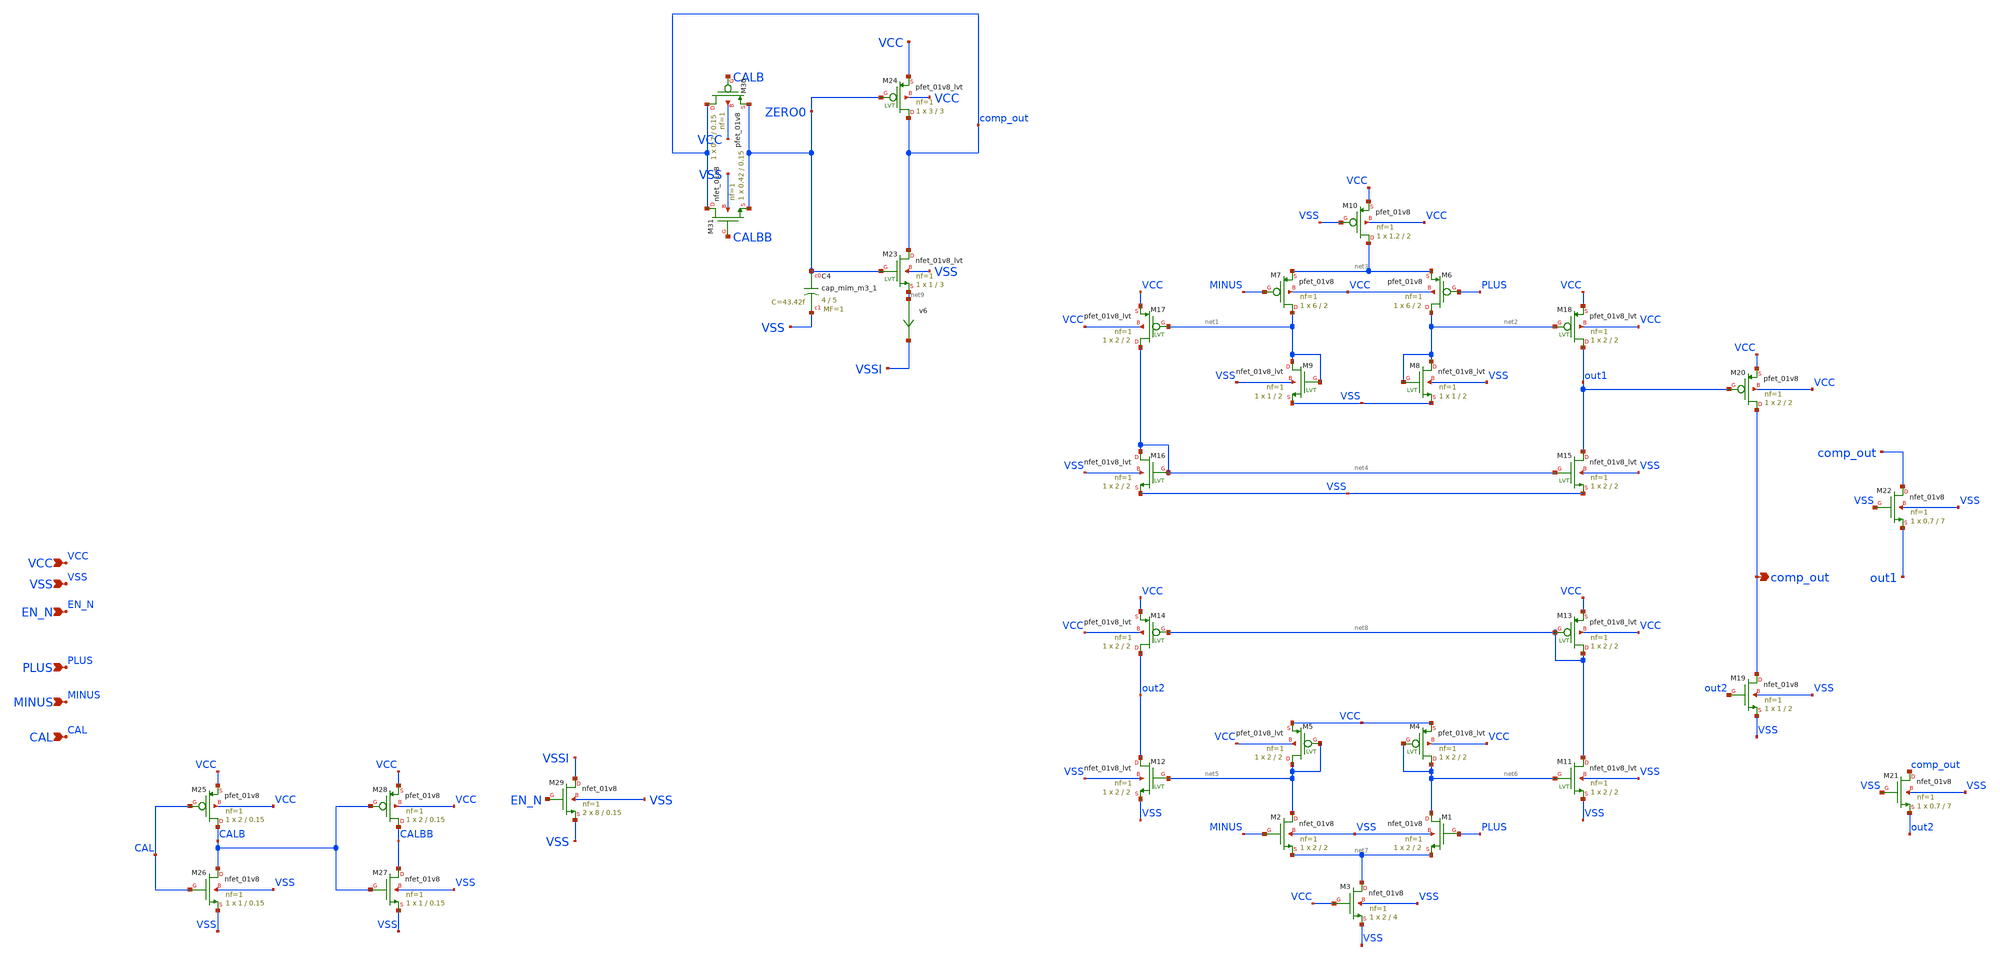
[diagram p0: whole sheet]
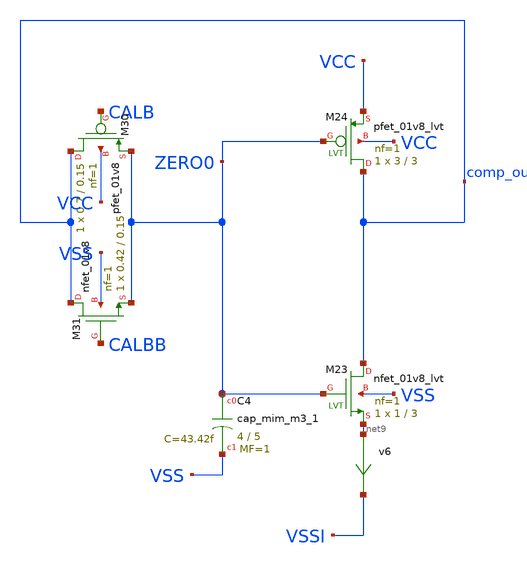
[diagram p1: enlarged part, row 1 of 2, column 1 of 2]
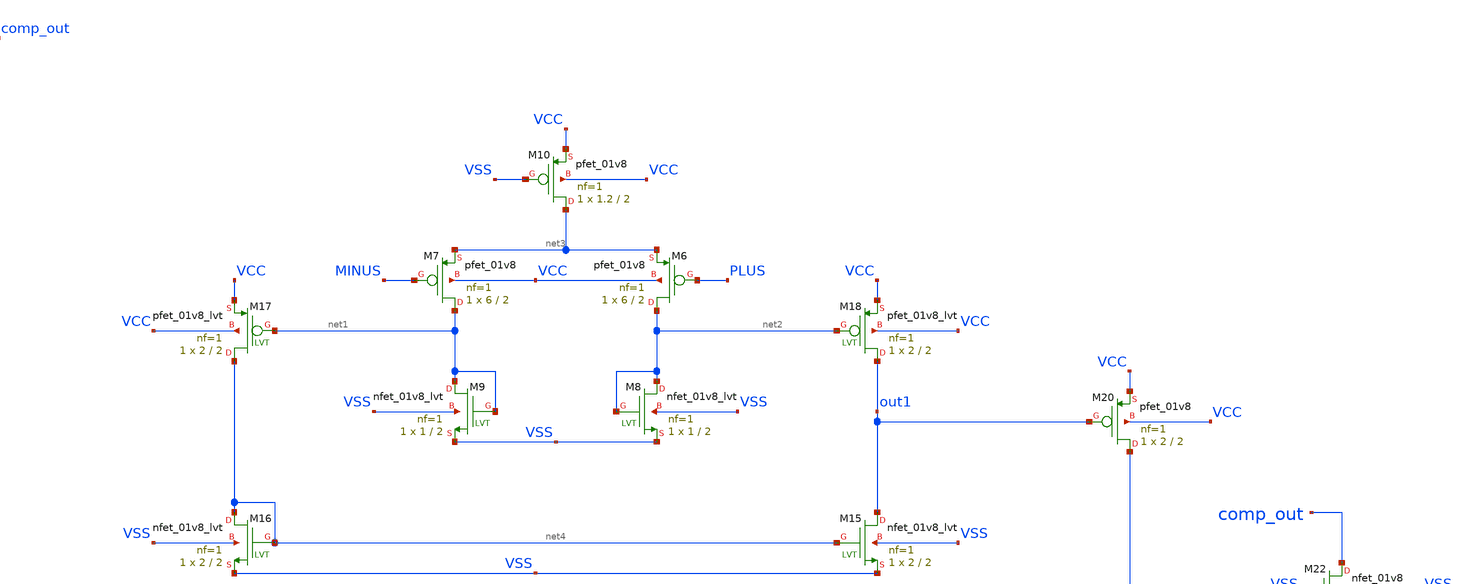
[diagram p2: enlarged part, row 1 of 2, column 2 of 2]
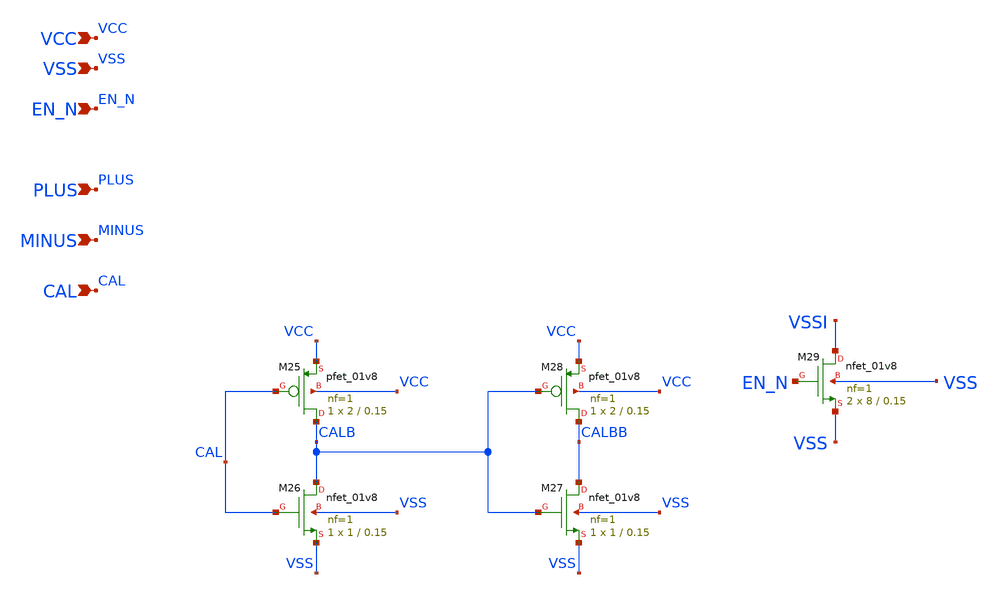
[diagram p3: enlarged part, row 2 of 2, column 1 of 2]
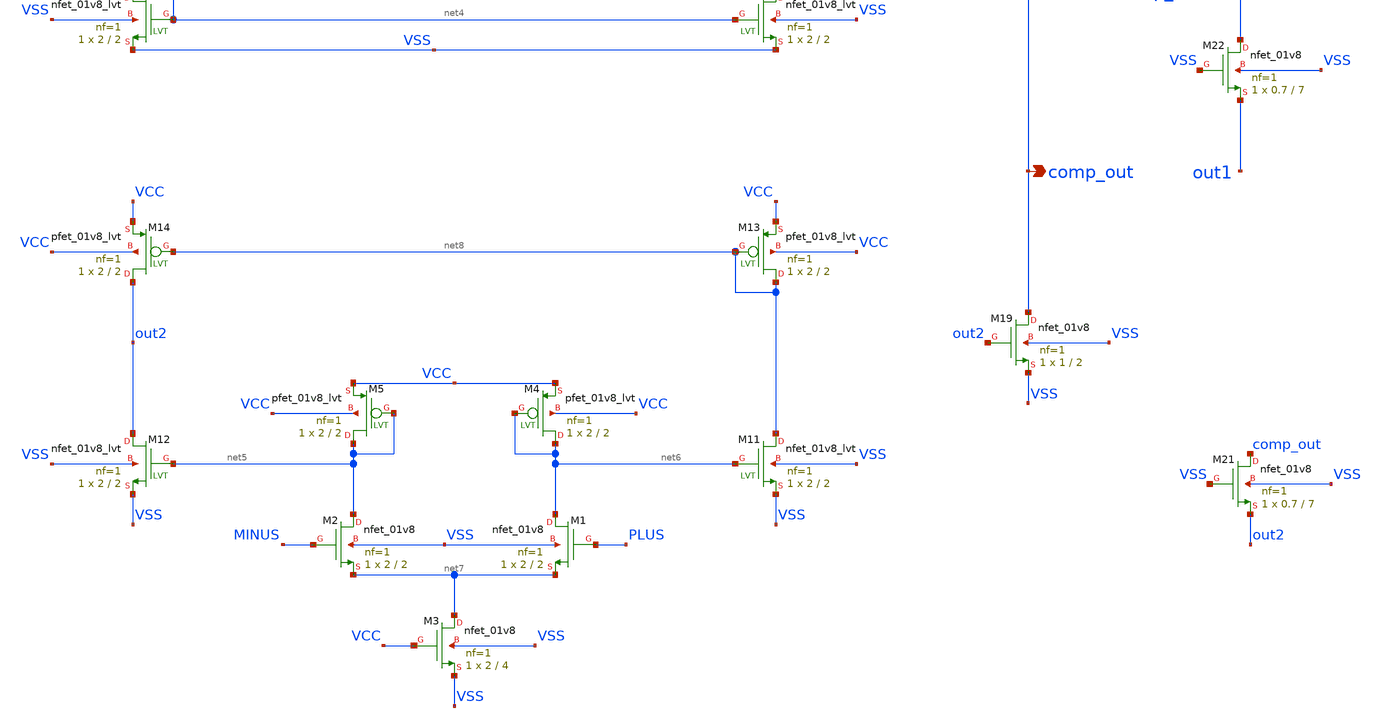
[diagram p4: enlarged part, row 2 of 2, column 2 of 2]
** sch_path: xschem/comparator.sch
**.subckt comparator VCC VSS EN_N PLUS MINUS comp_out CAL
*.ipin VCC
*.ipin VSS
*.ipin EN_N
*.ipin PLUS
*.ipin MINUS
*.opin comp_out
*.ipin CAL
v6 net9 VSSI 0
.save i(v6)
XC4 ZERO0 VSS sky130_fd_pr__cap_mim_m3_1 W=4 L=5 MF=1 m=1
XM1 net6 PLUS net7 VSS sky130_fd_pr__nfet_01v8 L=2 W=2 nf=1 ad='int((nf+1)/2) * W/nf * 0.29' as='int((nf+2)/2) * W/nf * 0.29'
+ pd='2*int((nf+1)/2) * (W/nf + 0.29)' ps='2*int((nf+2)/2) * (W/nf + 0.29)' nrd='0.29 / W' nrs='0.29 / W'
+ sa=0 sb=0 sd=0 mult=1 m=1
XM2 net5 MINUS net7 VSS sky130_fd_pr__nfet_01v8 L=2 W=2 nf=1 ad='int((nf+1)/2) * W/nf * 0.29' as='int((nf+2)/2) * W/nf * 0.29'
+ pd='2*int((nf+1)/2) * (W/nf + 0.29)' ps='2*int((nf+2)/2) * (W/nf + 0.29)' nrd='0.29 / W' nrs='0.29 / W'
+ sa=0 sb=0 sd=0 mult=1 m=1
XM3 net7 VCC VSS VSS sky130_fd_pr__nfet_01v8 L=4 W=2 nf=1 ad='int((nf+1)/2) * W/nf * 0.29' as='int((nf+2)/2) * W/nf * 0.29'
+ pd='2*int((nf+1)/2) * (W/nf + 0.29)' ps='2*int((nf+2)/2) * (W/nf + 0.29)' nrd='0.29 / W' nrs='0.29 / W'
+ sa=0 sb=0 sd=0 mult=1 m=1
XM4 net6 net6 VCC VCC sky130_fd_pr__pfet_01v8_lvt L=2 W=2 nf=1 ad='int((nf+1)/2) * W/nf * 0.29' as='int((nf+2)/2) * W/nf * 0.29'
+ pd='2*int((nf+1)/2) * (W/nf + 0.29)' ps='2*int((nf+2)/2) * (W/nf + 0.29)' nrd='0.29 / W' nrs='0.29 / W'
+ sa=0 sb=0 sd=0 mult=1 m=1
XM5 net5 net5 VCC VCC sky130_fd_pr__pfet_01v8_lvt L=2 W=2 nf=1 ad='int((nf+1)/2) * W/nf * 0.29' as='int((nf+2)/2) * W/nf * 0.29'
+ pd='2*int((nf+1)/2) * (W/nf + 0.29)' ps='2*int((nf+2)/2) * (W/nf + 0.29)' nrd='0.29 / W' nrs='0.29 / W'
+ sa=0 sb=0 sd=0 mult=1 m=1
XM6 net2 PLUS net3 VCC sky130_fd_pr__pfet_01v8 L=2 W=6 nf=1 ad='int((nf+1)/2) * W/nf * 0.29' as='int((nf+2)/2) * W/nf * 0.29'
+ pd='2*int((nf+1)/2) * (W/nf + 0.29)' ps='2*int((nf+2)/2) * (W/nf + 0.29)' nrd='0.29 / W' nrs='0.29 / W'
+ sa=0 sb=0 sd=0 mult=1 m=1
XM7 net1 MINUS net3 VCC sky130_fd_pr__pfet_01v8 L=2 W=6 nf=1 ad='int((nf+1)/2) * W/nf * 0.29' as='int((nf+2)/2) * W/nf * 0.29'
+ pd='2*int((nf+1)/2) * (W/nf + 0.29)' ps='2*int((nf+2)/2) * (W/nf + 0.29)' nrd='0.29 / W' nrs='0.29 / W'
+ sa=0 sb=0 sd=0 mult=1 m=1
XM8 net2 net2 VSS VSS sky130_fd_pr__nfet_01v8_lvt L=2 W=1 nf=1 ad='int((nf+1)/2) * W/nf * 0.29' as='int((nf+2)/2) * W/nf * 0.29'
+ pd='2*int((nf+1)/2) * (W/nf + 0.29)' ps='2*int((nf+2)/2) * (W/nf + 0.29)' nrd='0.29 / W' nrs='0.29 / W'
+ sa=0 sb=0 sd=0 mult=1 m=1
XM9 net1 net1 VSS VSS sky130_fd_pr__nfet_01v8_lvt L=2 W=1 nf=1 ad='int((nf+1)/2) * W/nf * 0.29' as='int((nf+2)/2) * W/nf * 0.29'
+ pd='2*int((nf+1)/2) * (W/nf + 0.29)' ps='2*int((nf+2)/2) * (W/nf + 0.29)' nrd='0.29 / W' nrs='0.29 / W'
+ sa=0 sb=0 sd=0 mult=1 m=1
XM10 net3 VSS VCC VCC sky130_fd_pr__pfet_01v8 L=2 W=1.2 nf=1 ad='int((nf+1)/2) * W/nf * 0.29' as='int((nf+2)/2) * W/nf * 0.29'
+ pd='2*int((nf+1)/2) * (W/nf + 0.29)' ps='2*int((nf+2)/2) * (W/nf + 0.29)' nrd='0.29 / W' nrs='0.29 / W'
+ sa=0 sb=0 sd=0 mult=1 m=1
XM14 out2 net8 VCC VCC sky130_fd_pr__pfet_01v8_lvt L=2 W=2 nf=1 ad='int((nf+1)/2) * W/nf * 0.29' as='int((nf+2)/2) * W/nf * 0.29'
+ pd='2*int((nf+1)/2) * (W/nf + 0.29)' ps='2*int((nf+2)/2) * (W/nf + 0.29)' nrd='0.29 / W' nrs='0.29 / W'
+ sa=0 sb=0 sd=0 mult=1 m=1
XM11 net8 net6 VSS VSS sky130_fd_pr__nfet_01v8_lvt L=2 W=2 nf=1 ad='int((nf+1)/2) * W/nf * 0.29' as='int((nf+2)/2) * W/nf * 0.29'
+ pd='2*int((nf+1)/2) * (W/nf + 0.29)' ps='2*int((nf+2)/2) * (W/nf + 0.29)' nrd='0.29 / W' nrs='0.29 / W'
+ sa=0 sb=0 sd=0 mult=1 m=1
XM12 out2 net5 VSS VSS sky130_fd_pr__nfet_01v8_lvt L=2 W=2 nf=1 ad='int((nf+1)/2) * W/nf * 0.29' as='int((nf+2)/2) * W/nf * 0.29'
+ pd='2*int((nf+1)/2) * (W/nf + 0.29)' ps='2*int((nf+2)/2) * (W/nf + 0.29)' nrd='0.29 / W' nrs='0.29 / W'
+ sa=0 sb=0 sd=0 mult=1 m=1
XM13 net8 net8 VCC VCC sky130_fd_pr__pfet_01v8_lvt L=2 W=2 nf=1 ad='int((nf+1)/2) * W/nf * 0.29' as='int((nf+2)/2) * W/nf * 0.29'
+ pd='2*int((nf+1)/2) * (W/nf + 0.29)' ps='2*int((nf+2)/2) * (W/nf + 0.29)' nrd='0.29 / W' nrs='0.29 / W'
+ sa=0 sb=0 sd=0 mult=1 m=1
XM15 out1 net4 VSS VSS sky130_fd_pr__nfet_01v8_lvt L=2 W=2 nf=1 ad='int((nf+1)/2) * W/nf * 0.29' as='int((nf+2)/2) * W/nf * 0.29'
+ pd='2*int((nf+1)/2) * (W/nf + 0.29)' ps='2*int((nf+2)/2) * (W/nf + 0.29)' nrd='0.29 / W' nrs='0.29 / W'
+ sa=0 sb=0 sd=0 mult=1 m=1
XM16 net4 net4 VSS VSS sky130_fd_pr__nfet_01v8_lvt L=2 W=2 nf=1 ad='int((nf+1)/2) * W/nf * 0.29' as='int((nf+2)/2) * W/nf * 0.29'
+ pd='2*int((nf+1)/2) * (W/nf + 0.29)' ps='2*int((nf+2)/2) * (W/nf + 0.29)' nrd='0.29 / W' nrs='0.29 / W'
+ sa=0 sb=0 sd=0 mult=1 m=1
XM17 net4 net1 VCC VCC sky130_fd_pr__pfet_01v8_lvt L=2 W=2 nf=1 ad='int((nf+1)/2) * W/nf * 0.29' as='int((nf+2)/2) * W/nf * 0.29'
+ pd='2*int((nf+1)/2) * (W/nf + 0.29)' ps='2*int((nf+2)/2) * (W/nf + 0.29)' nrd='0.29 / W' nrs='0.29 / W'
+ sa=0 sb=0 sd=0 mult=1 m=1
XM18 out1 net2 VCC VCC sky130_fd_pr__pfet_01v8_lvt L=2 W=2 nf=1 ad='int((nf+1)/2) * W/nf * 0.29' as='int((nf+2)/2) * W/nf * 0.29'
+ pd='2*int((nf+1)/2) * (W/nf + 0.29)' ps='2*int((nf+2)/2) * (W/nf + 0.29)' nrd='0.29 / W' nrs='0.29 / W'
+ sa=0 sb=0 sd=0 mult=1 m=1
XM19 comp_out out2 VSS VSS sky130_fd_pr__nfet_01v8 L=2 W=1 nf=1 ad='int((nf+1)/2) * W/nf * 0.29' as='int((nf+2)/2) * W/nf * 0.29'
+ pd='2*int((nf+1)/2) * (W/nf + 0.29)' ps='2*int((nf+2)/2) * (W/nf + 0.29)' nrd='0.29 / W' nrs='0.29 / W'
+ sa=0 sb=0 sd=0 mult=1 m=1
XM20 comp_out out1 VCC VCC sky130_fd_pr__pfet_01v8 L=2 W=2 nf=1 ad='int((nf+1)/2) * W/nf * 0.29' as='int((nf+2)/2) * W/nf * 0.29'
+ pd='2*int((nf+1)/2) * (W/nf + 0.29)' ps='2*int((nf+2)/2) * (W/nf + 0.29)' nrd='0.29 / W' nrs='0.29 / W'
+ sa=0 sb=0 sd=0 mult=1 m=1
XM21 comp_out VSS out2 VSS sky130_fd_pr__nfet_01v8 L=7 W=0.7 nf=1 ad='int((nf+1)/2) * W/nf * 0.29' as='int((nf+2)/2) * W/nf * 0.29'
+ pd='2*int((nf+1)/2) * (W/nf + 0.29)' ps='2*int((nf+2)/2) * (W/nf + 0.29)' nrd='0.29 / W' nrs='0.29 / W'
+ sa=0 sb=0 sd=0 mult=1 m=1
XM23 comp_out ZERO0 net9 VSS sky130_fd_pr__nfet_01v8_lvt L=3 W=1 nf=1 ad='W * 0.29' as='W * 0.29' pd='2*(W + 0.29)'
+ ps='2*(W + 0.29)' nrd=0 nrs=0 sa=0 sb=0 sd=0 mult=1 m=1
XM24 comp_out ZERO0 VCC VCC sky130_fd_pr__pfet_01v8_lvt L=3 W=3 nf=1 ad='W * 0.29' as='W * 0.29' pd='2*(W + 0.29)'
+ ps='2*(W + 0.29)' nrd=0 nrs=0 sa=0 sb=0 sd=0 mult=1 m=1
XM25 CALB CAL VCC VCC sky130_fd_pr__pfet_01v8 L=0.15 W=2 nf=1 ad='int((nf+1)/2) * W/nf * 0.29' as='int((nf+2)/2) * W/nf * 0.29'
+ pd='2*int((nf+1)/2) * (W/nf + 0.29)' ps='2*int((nf+2)/2) * (W/nf + 0.29)' nrd='0.29 / W' nrs='0.29 / W'
+ sa=0 sb=0 sd=0 mult=1 m=1
XM26 CALB CAL VSS VSS sky130_fd_pr__nfet_01v8 L=0.15 W=1 nf=1 ad='int((nf+1)/2) * W/nf * 0.29' as='int((nf+2)/2) * W/nf * 0.29'
+ pd='2*int((nf+1)/2) * (W/nf + 0.29)' ps='2*int((nf+2)/2) * (W/nf + 0.29)' nrd='0.29 / W' nrs='0.29 / W'
+ sa=0 sb=0 sd=0 mult=1 m=1
XM27 CALBB CALB VSS VSS sky130_fd_pr__nfet_01v8 L=0.15 W=1 nf=1 ad='int((nf+1)/2) * W/nf * 0.29' as='int((nf+2)/2) * W/nf * 0.29'
+ pd='2*int((nf+1)/2) * (W/nf + 0.29)' ps='2*int((nf+2)/2) * (W/nf + 0.29)' nrd='0.29 / W' nrs='0.29 / W'
+ sa=0 sb=0 sd=0 mult=1 m=1
XM28 CALBB CALB VCC VCC sky130_fd_pr__pfet_01v8 L=0.15 W=2 nf=1 ad='int((nf+1)/2) * W/nf * 0.29' as='int((nf+2)/2) * W/nf * 0.29'
+ pd='2*int((nf+1)/2) * (W/nf + 0.29)' ps='2*int((nf+2)/2) * (W/nf + 0.29)' nrd='0.29 / W' nrs='0.29 / W'
+ sa=0 sb=0 sd=0 mult=1 m=1
XM29 VSSI EN_N VSS VSS sky130_fd_pr__nfet_01v8 L=0.15 W=8 nf=1 ad='W * 0.29' as='W * 0.29' pd='W + 2 * 0.29'
+ ps='W + 2 * 0.29' nrd=0 nrs=0 sa=0 sb=0 sd=0 mult=2 m=2
XM22 comp_out VSS out1 VSS sky130_fd_pr__nfet_01v8 L=7 W=0.7 nf=1 ad='int((nf+1)/2) * W/nf * 0.29' as='int((nf+2)/2) * W/nf * 0.29'
+ pd='2*int((nf+1)/2) * (W/nf + 0.29)' ps='2*int((nf+2)/2) * (W/nf + 0.29)' nrd='0.29 / W' nrs='0.29 / W'
+ sa=0 sb=0 sd=0 mult=1 m=1
XM30 comp_out CALB ZERO0 VCC sky130_fd_pr__pfet_01v8 L=0.15 W=0.7 nf=1 ad='int((nf+1)/2) * W/nf * 0.29'
+ as='int((nf+2)/2) * W/nf * 0.29' pd='2*int((nf+1)/2) * (W/nf + 0.29)' ps='2*int((nf+2)/2) * (W/nf + 0.29)'
+ nrd='0.29 / W' nrs='0.29 / W' sa=0 sb=0 sd=0 mult=1 m=1
XM31 comp_out CALBB ZERO0 VSS sky130_fd_pr__nfet_01v8 L=0.15 W=0.42 nf=1 ad='int((nf+1)/2) * W/nf * 0.29'
+ as='int((nf+2)/2) * W/nf * 0.29' pd='2*int((nf+1)/2) * (W/nf + 0.29)' ps='2*int((nf+2)/2) * (W/nf + 0.29)'
+ nrd='0.29 / W' nrs='0.29 / W' sa=0 sb=0 sd=0 mult=1 m=1
**.ends
.end
